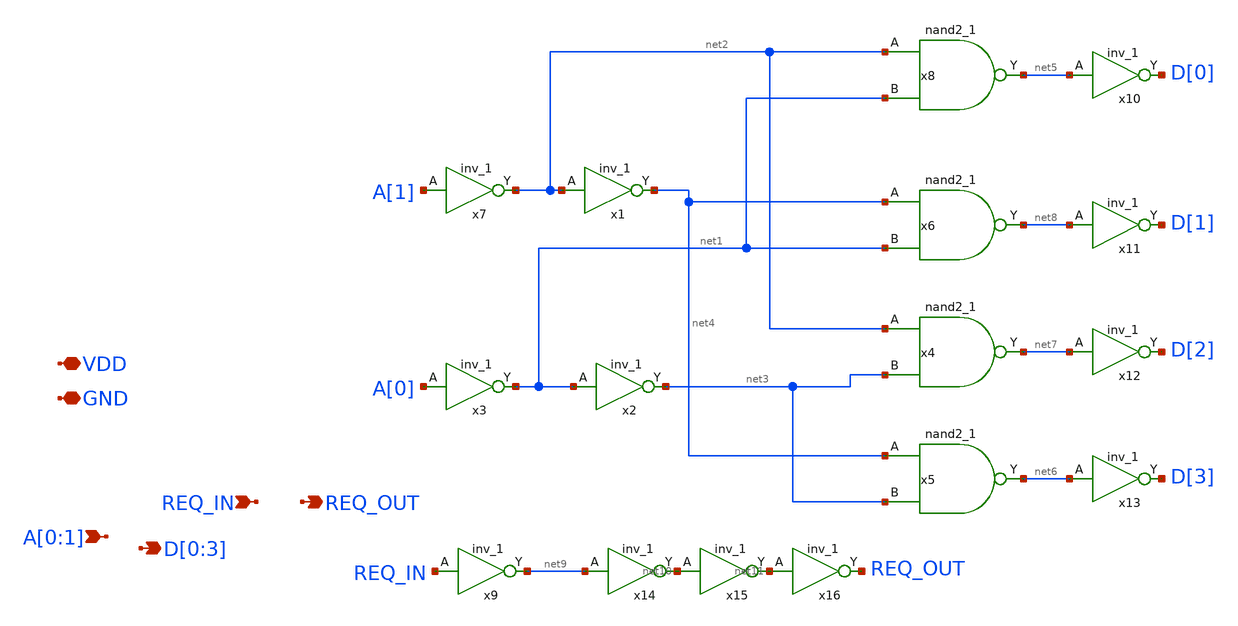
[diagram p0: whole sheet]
** sch_path: design/xschem/decoder_2_to_4.sch
**.subckt decoder_2_to_4 A[0],A[1] D[0],D[1],D[2],D[3] REQ_IN REQ_OUT VDD GND
*.ipin A[0],A[1]
*.opin D[0],D[1],D[2],D[3]
*.ipin REQ_IN
*.opin REQ_OUT
*.iopin VDD
*.iopin GND
x3 A[0] GND GND VDD VDD net1 sky130_fd_sc_hd__inv_1
x7 A[1] GND GND VDD VDD net2 sky130_fd_sc_hd__inv_1
x1 net2 GND GND VDD VDD net4 sky130_fd_sc_hd__inv_1
x2 net1 GND GND VDD VDD net3 sky130_fd_sc_hd__inv_1
x10 net5 GND GND VDD VDD D[0] sky130_fd_sc_hd__inv_1
x11 net8 GND GND VDD VDD D[1] sky130_fd_sc_hd__inv_1
x12 net7 GND GND VDD VDD D[2] sky130_fd_sc_hd__inv_1
x13 net6 GND GND VDD VDD D[3] sky130_fd_sc_hd__inv_1
x4 net2 net3 GND GND VDD VDD net7 sky130_fd_sc_hd__nand2_1
x5 net4 net3 GND GND VDD VDD net6 sky130_fd_sc_hd__nand2_1
x6 net4 net1 GND GND VDD VDD net8 sky130_fd_sc_hd__nand2_1
x8 net2 net1 GND GND VDD VDD net5 sky130_fd_sc_hd__nand2_1
x9 REQ_IN GND GND VDD VDD net9 sky130_fd_sc_hd__inv_1
x14 net9 GND GND VDD VDD net10 sky130_fd_sc_hd__inv_1
x15 net10 GND GND VDD VDD net11 sky130_fd_sc_hd__inv_1
x16 net11 GND GND VDD VDD REQ_OUT sky130_fd_sc_hd__inv_1
**.ends
.end
